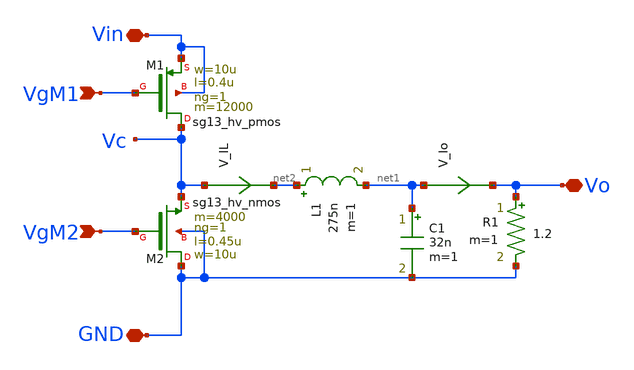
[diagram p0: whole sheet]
** sch_path: ChipUSM_AnalogTrack24/DCDCBuck/DCDC_Buck_V1p2.sch
**.subckt DCDC_Buck_V1p2 Vin VgM1 VgM2 Vo GND
*.iopin Vin
*.ipin VgM1
*.ipin VgM2
*.iopin Vo
*.iopin GND
XM2 GND VgM2 Vc GND sg13_hv_nmos w=10u l=0.45u ng=1 m=4000 mm_ok=1
XM1 Vc VgM1 Vin Vin sg13_hv_pmos w=10u l=0.4u ng=1 m=12000 mm_ok=1
L1 net2 net1 275n m=1
C1 net1 GND 32n m=1
V_Io net1 Vo 0
.save i(v_io)
V_IL Vc net2 0
.save i(v_il)
R1 Vo GND 1.2 m=1
**.ends
.end
